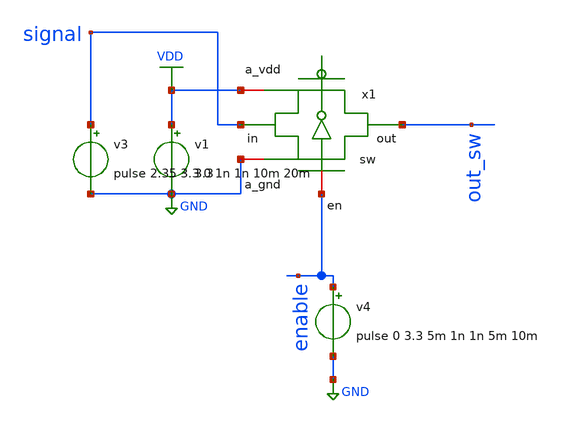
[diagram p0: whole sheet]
** sch_path: Schematics/ADC/simulations_elements/sim_sw.sch
**.subckt sim_sw
x1 GND VDD enable signal out_sw sw
v1 VDD GND 3.3
v4 enable GND pulse 0 3.3 5m 1n 1n 5m 10m
v3 signal GND pulse 2.35 3.3 0 1n 1n 10m 20m
**** begin user architecture code

** opencircuitdesign pdks install
.lib $::SKYWATER_MODELS/sky130.lib.spice tt

**** end user architecture code
**.ends
.GLOBAL GND
.GLOBAL VDD
**** begin user architecture code

* .option SCALE=1e-6
.option method=gear seed=12
.control
save all
tran 0.1m 30m
write sim_sw.raw
plot enable out_sw
.endc


**** end user architecture code
.end
